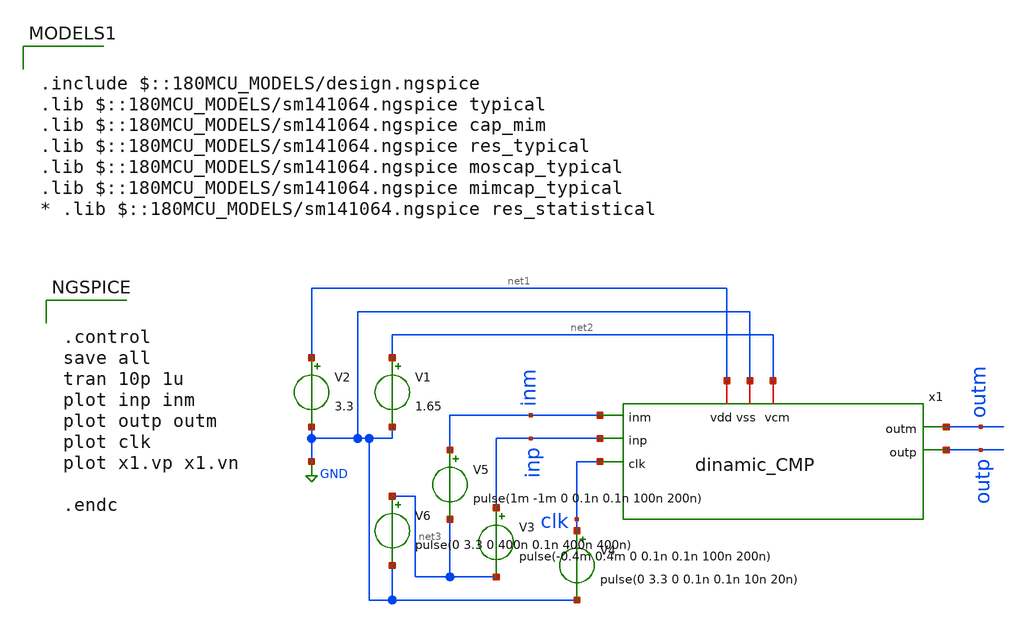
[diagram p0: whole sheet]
** sch_path: member_project/ice458/dynamic_comparator/xschem/dinamic_CMP_tb.sch
**.subckt dinamic_CMP_tb
x1 net1 GND net2 inm inp clk outm outp dinamic_CMP
V2 net1 GND 3.3
V1 net2 GND 1.65
V4 clk GND pulse(0 3.3 0 0.1n 0.1n 10n 20n)
V5 inm net3 pulse(1m -1m 0 0.1n 0.1n 100n 200n)
V3 inp net3 pulse(-0.4m 0.4m 0 0.1n 0.1n 100n 200n)
V6 net3 GND pulse(0 3.3 0 400n 0.1n 400n 400n)
**** begin user architecture code


.control
save all
tran 10p 1u
plot inp inm
plot outp outm
plot clk
plot x1.vp x1.vn

.endc



.include $::180MCU_MODELS/design.ngspice
.lib $::180MCU_MODELS/sm141064.ngspice typical
.lib $::180MCU_MODELS/sm141064.ngspice cap_mim
.lib $::180MCU_MODELS/sm141064.ngspice res_typical
.lib $::180MCU_MODELS/sm141064.ngspice moscap_typical
.lib $::180MCU_MODELS/sm141064.ngspice mimcap_typical
* .lib $::180MCU_MODELS/sm141064.ngspice res_statistical

**** end user architecture code
**.ends
.GLOBAL GND
.end
